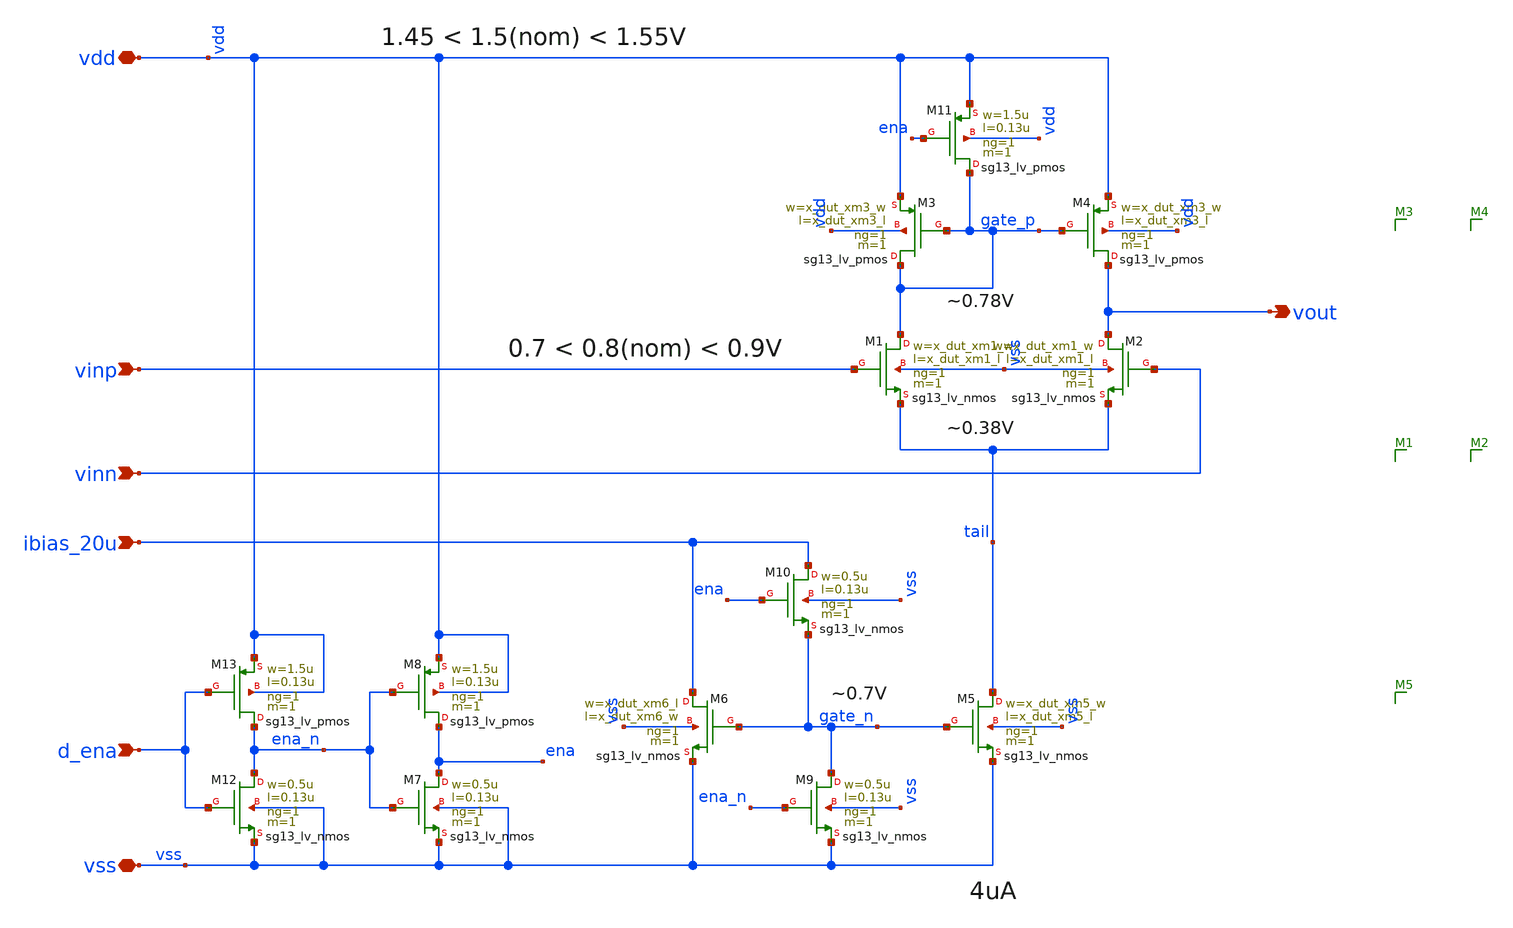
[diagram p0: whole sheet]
** sch_path: analog-db/circuits/amp_001_5t/pdk/ihp-sg13g2/schematic/ota-5t.sch
* (c) 2024-2025 H. Pretl, Apache-2.0 license
**.subckt ota-5t ibias_20u vdd vss vinp vinn vout d_ena
*.ipin ibias_20u
*.iopin vdd
*.iopin vss
*.ipin vinp
*.ipin vinn
*.opin vout
*.ipin d_ena
XM5 tail gate_n vss vss sg13_lv_nmos w=x_dut_xm5_w l=x_dut_xm5_l ng=1 m=1 mm_ok=1
XM4 vout gate_p vdd vdd sg13_lv_pmos w=x_dut_xm3_w l=x_dut_xm3_l ng=1 m=1 mm_ok=1
XM1 gate_p vinp tail vss sg13_lv_nmos w=x_dut_xm1_w l=x_dut_xm1_l ng=1 m=1 mm_ok=1
XM2 vout vinn tail vss sg13_lv_nmos w=x_dut_xm1_w l=x_dut_xm1_l ng=1 m=1 mm_ok=1
XM3 gate_p gate_p vdd vdd sg13_lv_pmos w=x_dut_xm3_w l=x_dut_xm3_l ng=1 m=1 mm_ok=1
XM6 ibias_20u gate_n vss vss sg13_lv_nmos w=x_dut_xm6_l l=x_dut_xm6_w ng=1 m=1 mm_ok=1
XM9 gate_n ena_n vss vss sg13_lv_nmos w=0.5u l=0.13u ng=1 m=1 mm_ok=1
XM11 gate_p ena vdd vdd sg13_lv_pmos w=1.5u l=0.13u ng=1 m=1 mm_ok=1
XM7 ena ena_n vss vss sg13_lv_nmos w=0.5u l=0.13u ng=1 m=1 mm_ok=1
XM8 ena ena_n vdd vdd sg13_lv_pmos w=1.5u l=0.13u ng=1 m=1 mm_ok=1
XM10 ibias_20u ena gate_n vss sg13_lv_nmos w=0.5u l=0.13u ng=1 m=1 mm_ok=1
XM12 ena_n d_ena vss vss sg13_lv_nmos w=0.5u l=0.13u ng=1 m=1 mm_ok=1
XM13 ena_n d_ena vdd vdd sg13_lv_pmos w=1.5u l=0.13u ng=1 m=1 mm_ok=1
**.ends
.end
